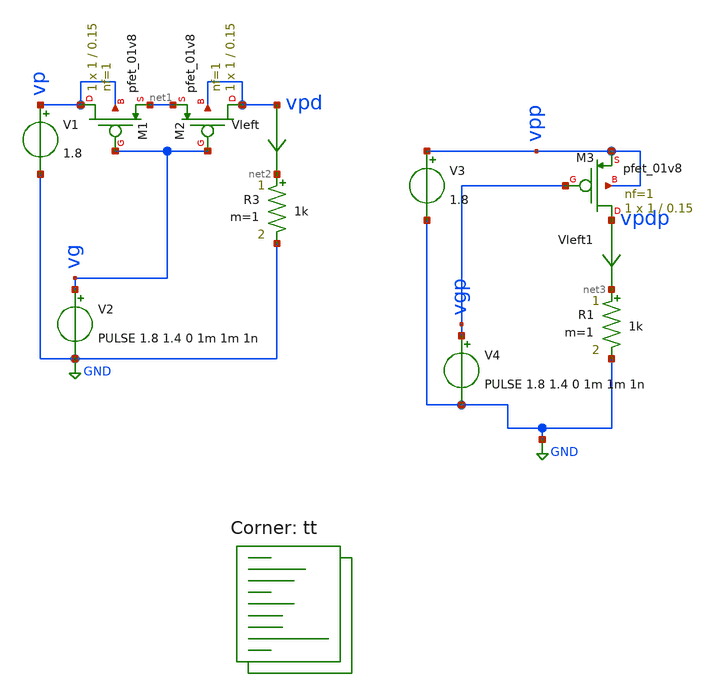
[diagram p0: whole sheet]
** sch_path: Schematics/mos_resistors/ig_dual_mpos.sch
**.subckt ig_dual_mpos
V1 vp GND 1.8
.save i(v1)
V2 vg GND PULSE 1.8 1.4 0 1m 1m 1n
.save i(v2)
XM1 vp vg net1 vp sky130_fd_pr__pfet_01v8 L=0.15 W=1 nf=1 ad='int((nf+1)/2) * W/nf * 0.29' as='int((nf+2)/2) * W/nf * 0.29'
+ pd='2*int((nf+1)/2) * (W/nf + 0.29)' ps='2*int((nf+2)/2) * (W/nf + 0.29)' nrd='0.29 / W' nrs='0.29 / W'
+ sa=0 sb=0 sd=0 mult=1 m=1
Vleft vpd net2 0
.save i(vleft)
R3 net2 GND 1k m=1
XM2 vpd vg net1 vpd sky130_fd_pr__pfet_01v8 L=0.15 W=1 nf=1 ad='int((nf+1)/2) * W/nf * 0.29' as='int((nf+2)/2) * W/nf * 0.29'
+ pd='2*int((nf+1)/2) * (W/nf + 0.29)' ps='2*int((nf+2)/2) * (W/nf + 0.29)' nrd='0.29 / W' nrs='0.29 / W'
+ sa=0 sb=0 sd=0 mult=1 m=1
V3 vpp GND 1.8
.save i(v3)
V4 vgp GND PULSE 1.8 1.4 0 1m 1m 1n
.save i(v4)
XM3 vpdp vgp vpp vpp sky130_fd_pr__pfet_01v8 L=0.15 W=1 nf=1 ad='int((nf+1)/2) * W/nf * 0.29' as='int((nf+2)/2) * W/nf * 0.29'
+ pd='2*int((nf+1)/2) * (W/nf + 0.29)' ps='2*int((nf+2)/2) * (W/nf + 0.29)' nrd='0.29 / W' nrs='0.29 / W'
+ sa=0 sb=0 sd=0 mult=1 m=1
Vleft1 vpdp net3 0
.save i(vleft1)
R1 net3 GND 1k m=1
**** begin user architecture code
.lib $::SKYWATER_MODELS/sky130.lib.spice tt
**** end user architecture code
**.ends
.GLOBAL GND
**** begin user architecture code

*.options savecurrents
.tran 10u 2m
.save all
.control
	run
	write ig_dual_mpos.raw
.endc


**** end user architecture code
.end
